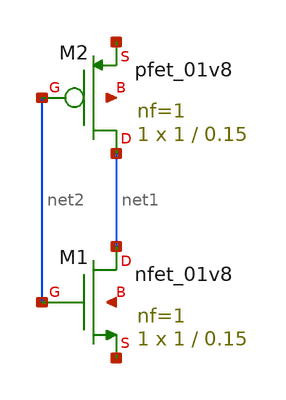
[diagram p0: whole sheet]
** sch_path: xschem/xschemfiles/hi.sch
**.subckt hi
XM1 net1 net2 net3 net4 sky130_fd_pr__nfet_01v8 L=0.15 W=1 nf=1 ad='int((nf+1)/2) * W/nf * 0.29' as='int((nf+2)/2) * W/nf * 0.29'
+ pd='2*int((nf+1)/2) * (W/nf + 0.29)' ps='2*int((nf+2)/2) * (W/nf + 0.29)' nrd='0.29 / W' nrs='0.29 / W'
+ sa=0 sb=0 sd=0 mult=1 m=1
XM2 net1 net2 net5 net6 sky130_fd_pr__pfet_01v8 L=0.15 W=1 nf=1 ad='int((nf+1)/2) * W/nf * 0.29' as='int((nf+2)/2) * W/nf * 0.29'
+ pd='2*int((nf+1)/2) * (W/nf + 0.29)' ps='2*int((nf+2)/2) * (W/nf + 0.29)' nrd='0.29 / W' nrs='0.29 / W'
+ sa=0 sb=0 sd=0 mult=1 m=1
**.ends
.end
